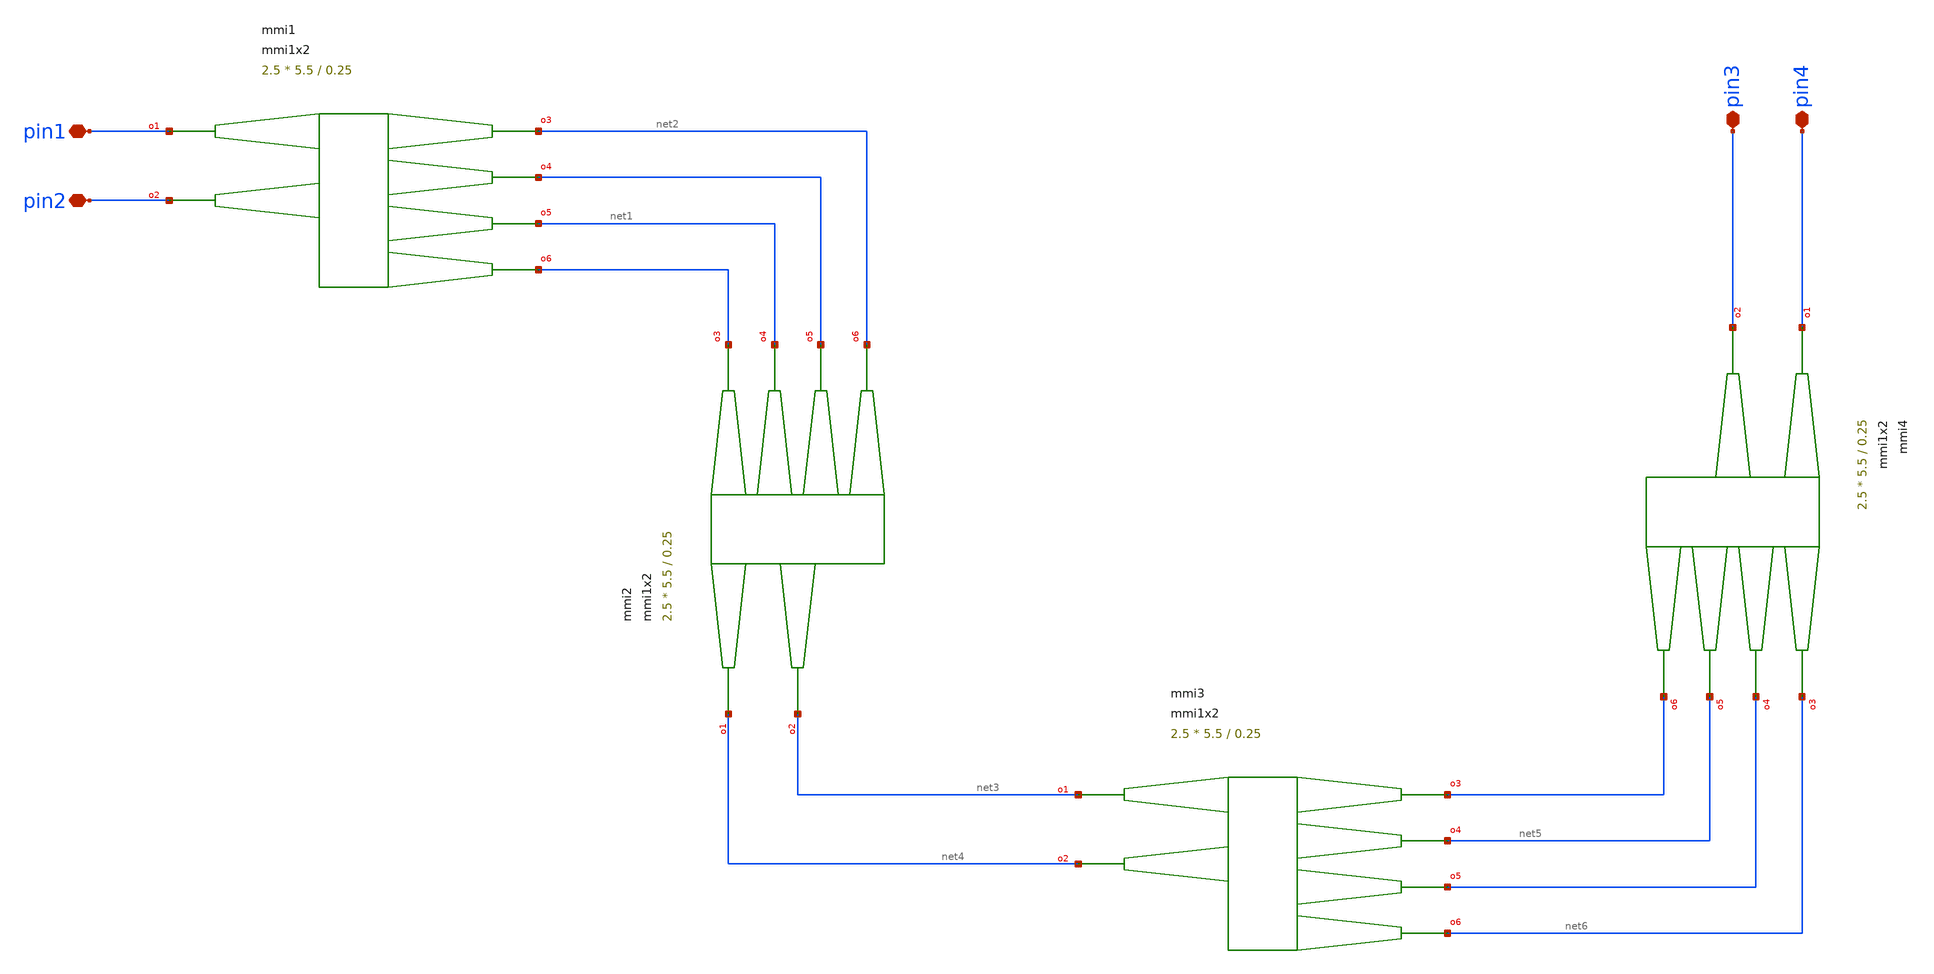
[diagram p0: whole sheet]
** sch_path: cells/xschem/tests/test_mmi_90degree_hybrid.sch
* SPDX-FileCopyrightText: 2023 Mabrains Company
* Licensed under the GNU GENERAL PUBLIC License, Version 3.0 (the "License");
* you may not use this file except in compliance with the License.
* GNU GENERAL PUBLIC LICENSE
* Version 3, 29 June 2007
* This program is free software: you can redistribute it and/or modify
* it under the terms of the GNU General Public License as published
* by the Free Software Foundation, either 3 of the License, or
* (at your option) any later version.
* This program is distributed in the hope that it will be useful,
* but WITHOUT ANY WARRANTY; without even the implied warranty of
* MERCHANTABILITY or FITNESS FOR A PARTICULAR PURPOSE.  See the
* GNU General Public License for more details.
* You should have received a copy of the GNU General Public License
* along with this program.  If not, see <https://www.gnu.org/licenses/>.
* SPDX-License-Identifier: GPL-3.0
**.subckt test_mmi_90degree_hybrid pin1 pin2 pin3 pin4
*.iopin pin1
*.iopin pin2
*.iopin pin3
*.iopin pin4
Pmmi1 pin1 pin2 net2 net1 net1 mmi1x2 width=0.5 width_taper=1 length_taper=10 length_mmi=5.5
+ width_mmi=2.5 gap_mmi=0.25
Pmmi2 net4 net3 net1 net2 net2 mmi1x2 width=0.5 width_taper=1 length_taper=10 length_mmi=5.5
+ width_mmi=2.5 gap_mmi=0.25
Pmmi3 net3 net4 net5 net6 net6 mmi1x2 width=0.5 width_taper=1 length_taper=10 length_mmi=5.5
+ width_mmi=2.5 gap_mmi=0.25
Pmmi4 pin4 pin3 net6 net5 net5 mmi1x2 width=0.5 width_taper=1 length_taper=10 length_mmi=5.5
+ width_mmi=2.5 gap_mmi=0.25
**.ends
.end
